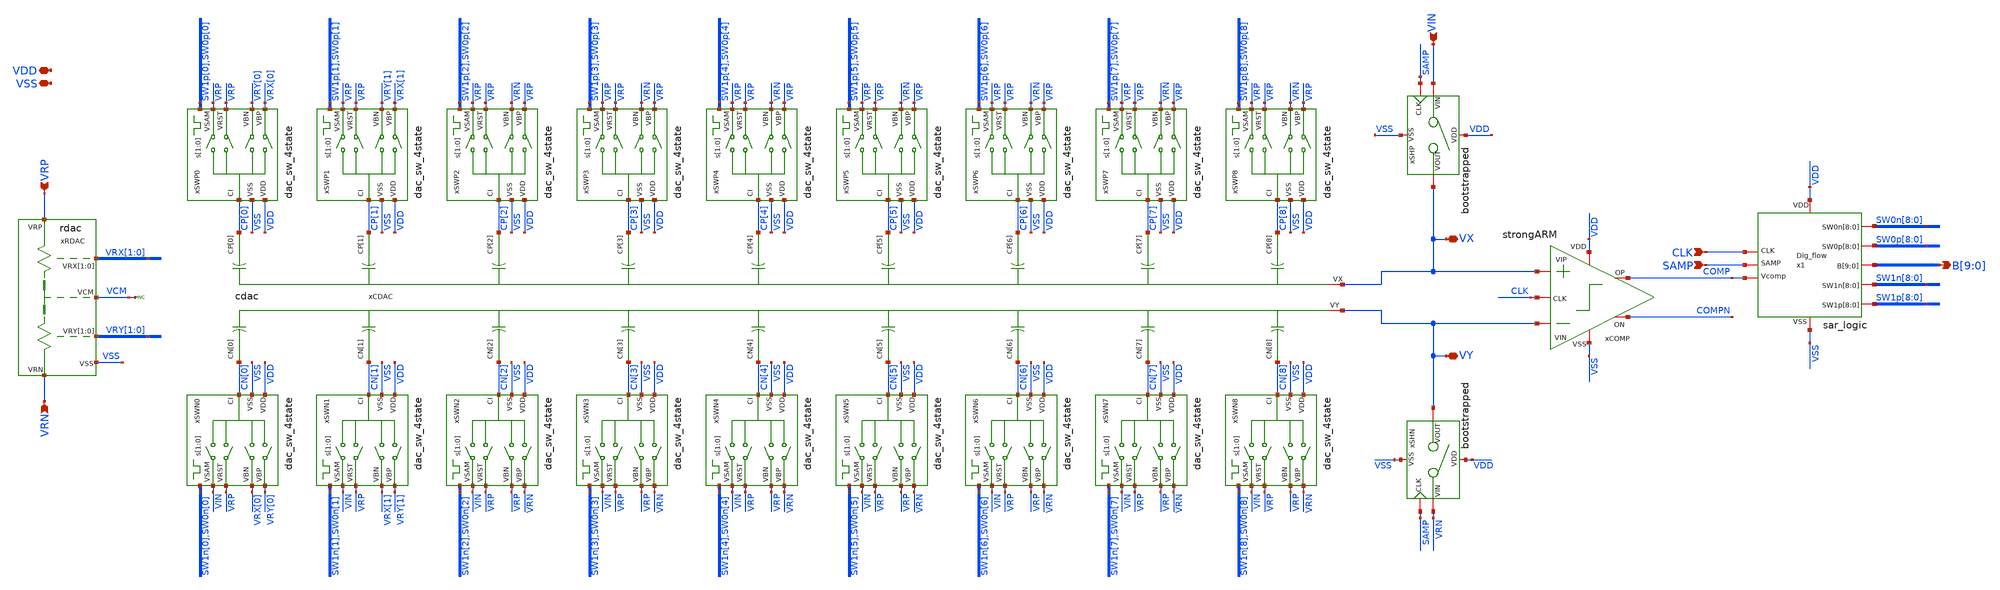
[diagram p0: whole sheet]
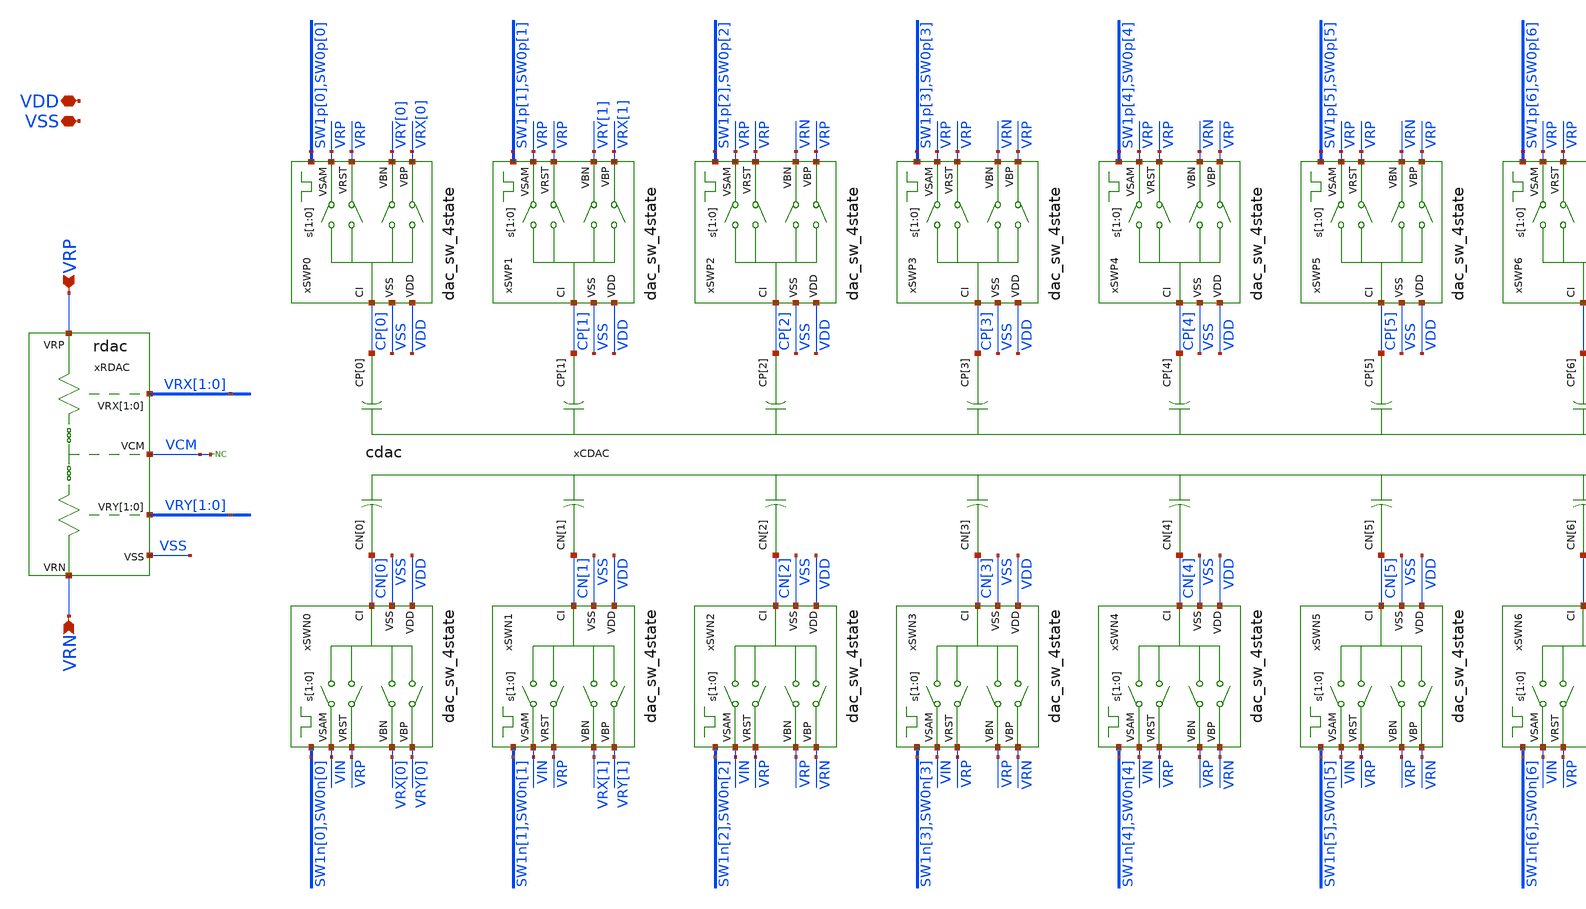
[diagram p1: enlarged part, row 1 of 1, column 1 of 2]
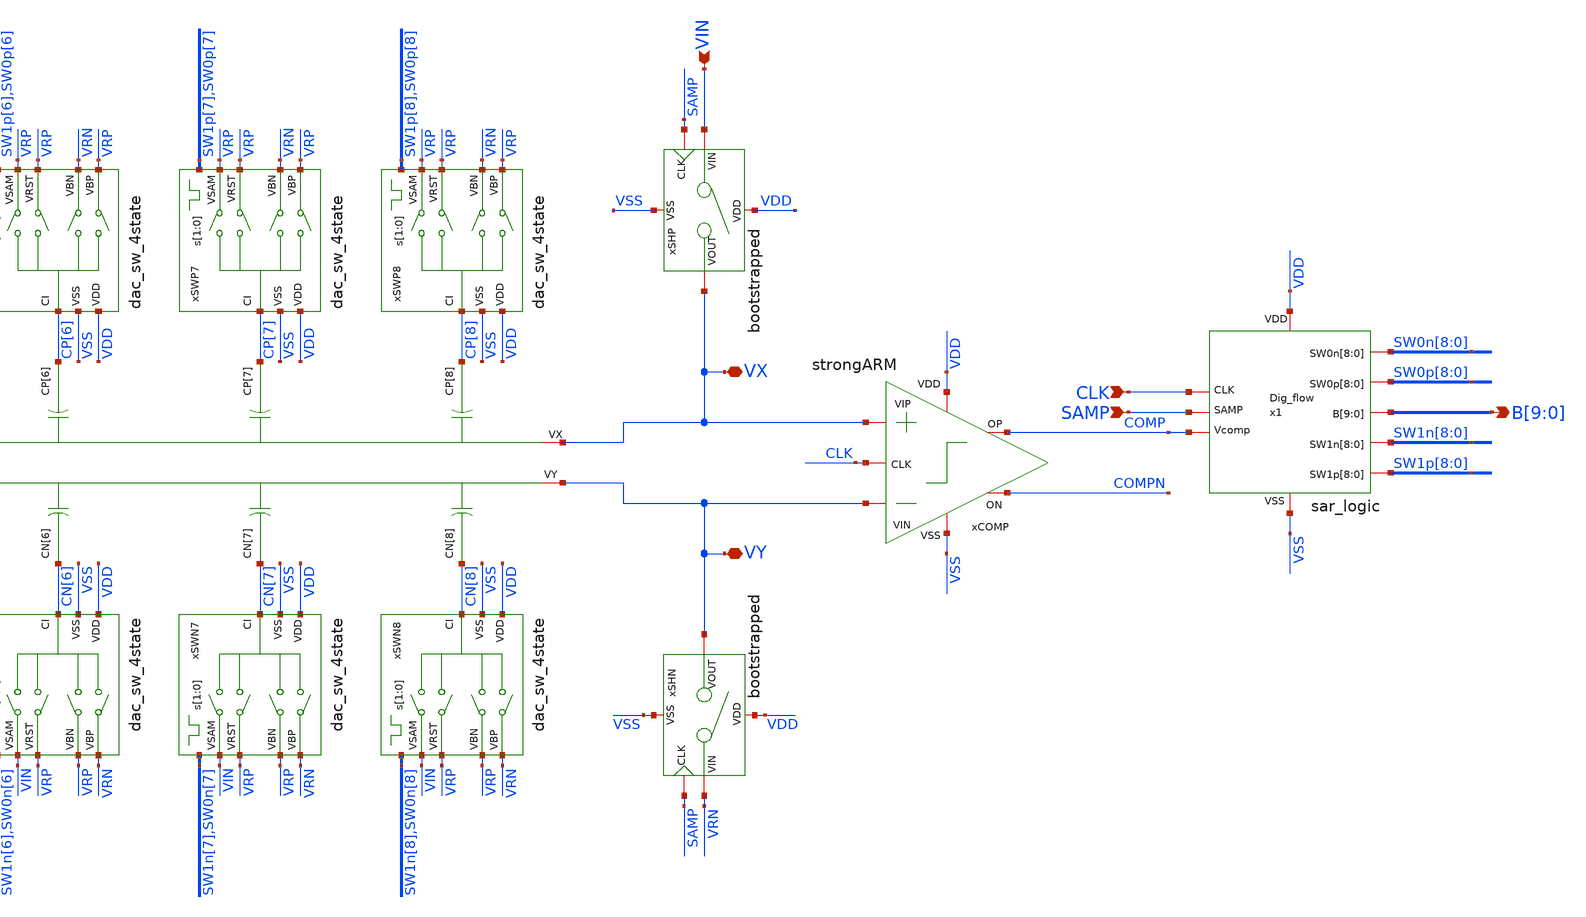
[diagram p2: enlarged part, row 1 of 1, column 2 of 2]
** sch_path: designs/sar_adc/top/sar_adc_10b/xschem/sar_adc_10b_digflow.sch
**.subckt sar_adc_10b_digflow VSS VDD VRP VRN CLK SAMP
*+ B[9],B[8],B[7],B[6],B[5],B[4],B[3],B[2],B[1],B[0] VIN VY VX
*.iopin VSS
*.iopin VDD
*.ipin VRP
*.ipin VRN
*.ipin CLK
*.ipin SAMP
*.opin B[9],B[8],B[7],B[6],B[5],B[4],B[3],B[2],B[1],B[0]
*.ipin VIN
*.iopin VY
*.iopin VX
xCDAC CP[8] CP[3] CP[5] CP[1] CP[0] CP[4] CP[6] CP[7] CP[2] CN[2] CN[1] CN[3] CN[8] CN[7] CN[6]
+ CN[5] CN[4] CN[0] VX VY cdac
xRDAC VCM VRX[1] VRX[0] VRY[1] VRY[0] VRP VRN VSS rdac
xSWP0 VDD SW1p[0] SW0p[0] VSS CP[0] VRP VRX[0] VRY[0] VRP dac_sw_4state
xSWP1 VDD SW1p[1] SW0p[1] VSS CP[1] VRP VRX[1] VRY[1] VRP dac_sw_4state
xSWP2 VDD SW1p[2] SW0p[2] VSS CP[2] VRP VRP VRN VRP dac_sw_4state
xSWP3 VDD SW1p[3] SW0p[3] VSS CP[3] VRP VRP VRN VRP dac_sw_4state
xSWP4 VDD SW1p[4] SW0p[4] VSS CP[4] VRP VRP VRN VRP dac_sw_4state
xSWP5 VDD SW1p[5] SW0p[5] VSS CP[5] VRP VRP VRN VRP dac_sw_4state
xSWP6 VDD SW1p[6] SW0p[6] VSS CP[6] VRP VRP VRN VRP dac_sw_4state
xSWP7 VDD SW1p[7] SW0p[7] VSS CP[7] VRP VRP VRN VRP dac_sw_4state
xSWP8 VDD SW1p[8] SW0p[8] VSS CP[8] VRP VRP VRN VRP dac_sw_4state
xSWN0 VDD SW1n[0] SW0n[0] VSS CN[0] VIN VRY[0] VRX[0] VRP dac_sw_4state
xSWN1 VDD SW1n[1] SW0n[1] VSS CN[1] VIN VRY[1] VRX[1] VRP dac_sw_4state
xSWN2 VDD SW1n[2] SW0n[2] VSS CN[2] VIN VRN VRP VRP dac_sw_4state
xSWN3 VDD SW1n[3] SW0n[3] VSS CN[3] VIN VRN VRP VRP dac_sw_4state
xSWN4 VDD SW1n[4] SW0n[4] VSS CN[4] VIN VRN VRP VRP dac_sw_4state
xSWN5 VDD SW1n[5] SW0n[5] VSS CN[5] VIN VRN VRP VRP dac_sw_4state
xSWN6 VDD SW1n[6] SW0n[6] VSS CN[6] VIN VRN VRP VRP dac_sw_4state
xSWN7 VDD SW1n[7] SW0n[7] VSS CN[7] VIN VRN VRP VRP dac_sw_4state
xSWN8 VDD SW1n[8] SW0n[8] VSS CN[8] VIN VRN VRP VRP dac_sw_4state
* noconn VCM
xSHP VDD VSS SAMP VIN VX bootstrapped
xSHN VDD VSS SAMP VRN VY bootstrapped
xCOMP VDD CLK COMPN COMP VY VX VSS strongARM
x1 VDD CLK SAMP COMP SW0n[8] SW0n[7] SW0n[6] SW0n[5] SW0n[4] SW0n[3] SW0n[2] SW0n[1] SW0n[0] B[9]
+ B[8] B[7] B[6] B[5] B[4] B[3] B[2] B[1] B[0] SW1p[8] SW1p[7] SW1p[6] SW1p[5] SW1p[4] SW1p[3] SW1p[2]
+ SW1p[1] SW1p[0] VSS SW0p[8] SW0p[7] SW0p[6] SW0p[5] SW0p[4] SW0p[3] SW0p[2] SW0p[1] SW0p[0] SW1n[8] SW1n[7]
+ SW1n[6] SW1n[5] SW1n[4] SW1n[3] SW1n[2] SW1n[1] SW1n[0] sar_logic
**.ends
.end
